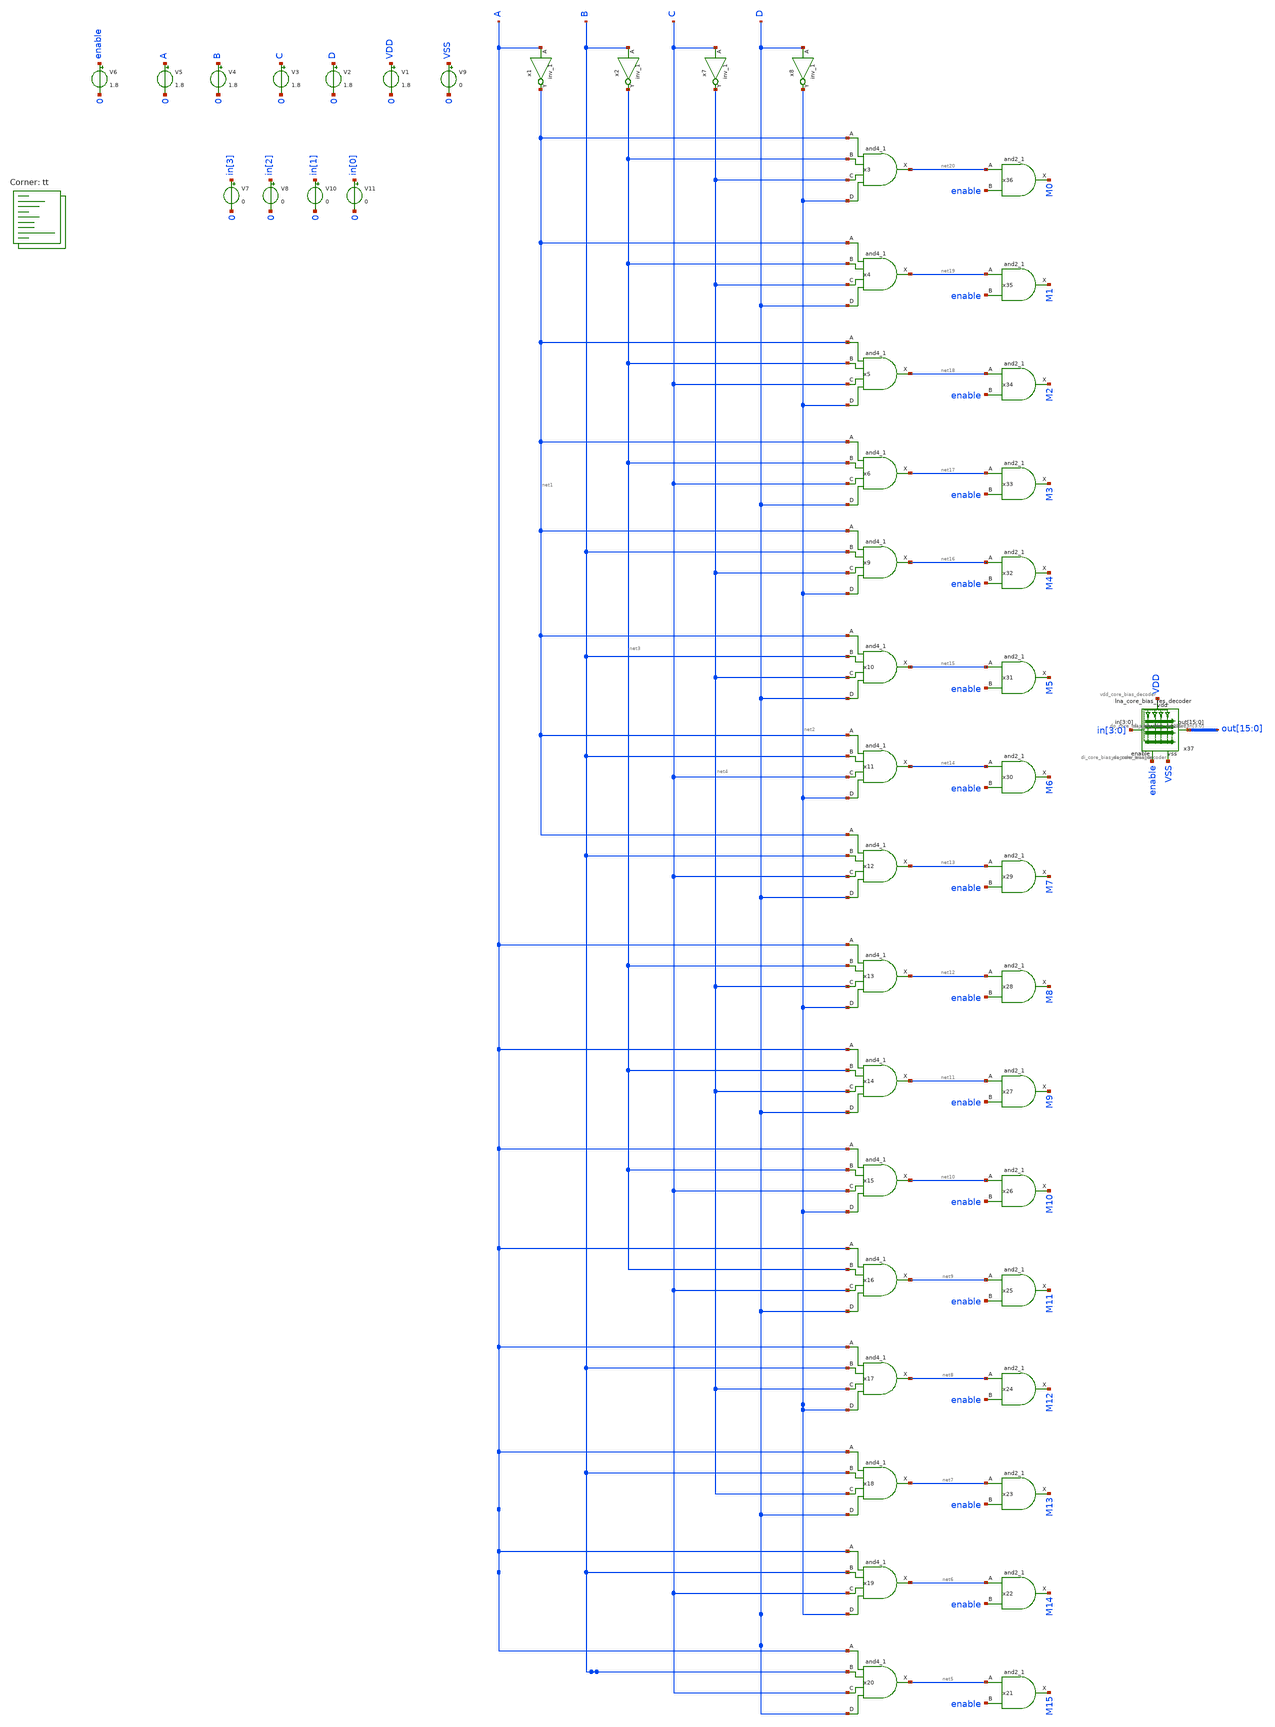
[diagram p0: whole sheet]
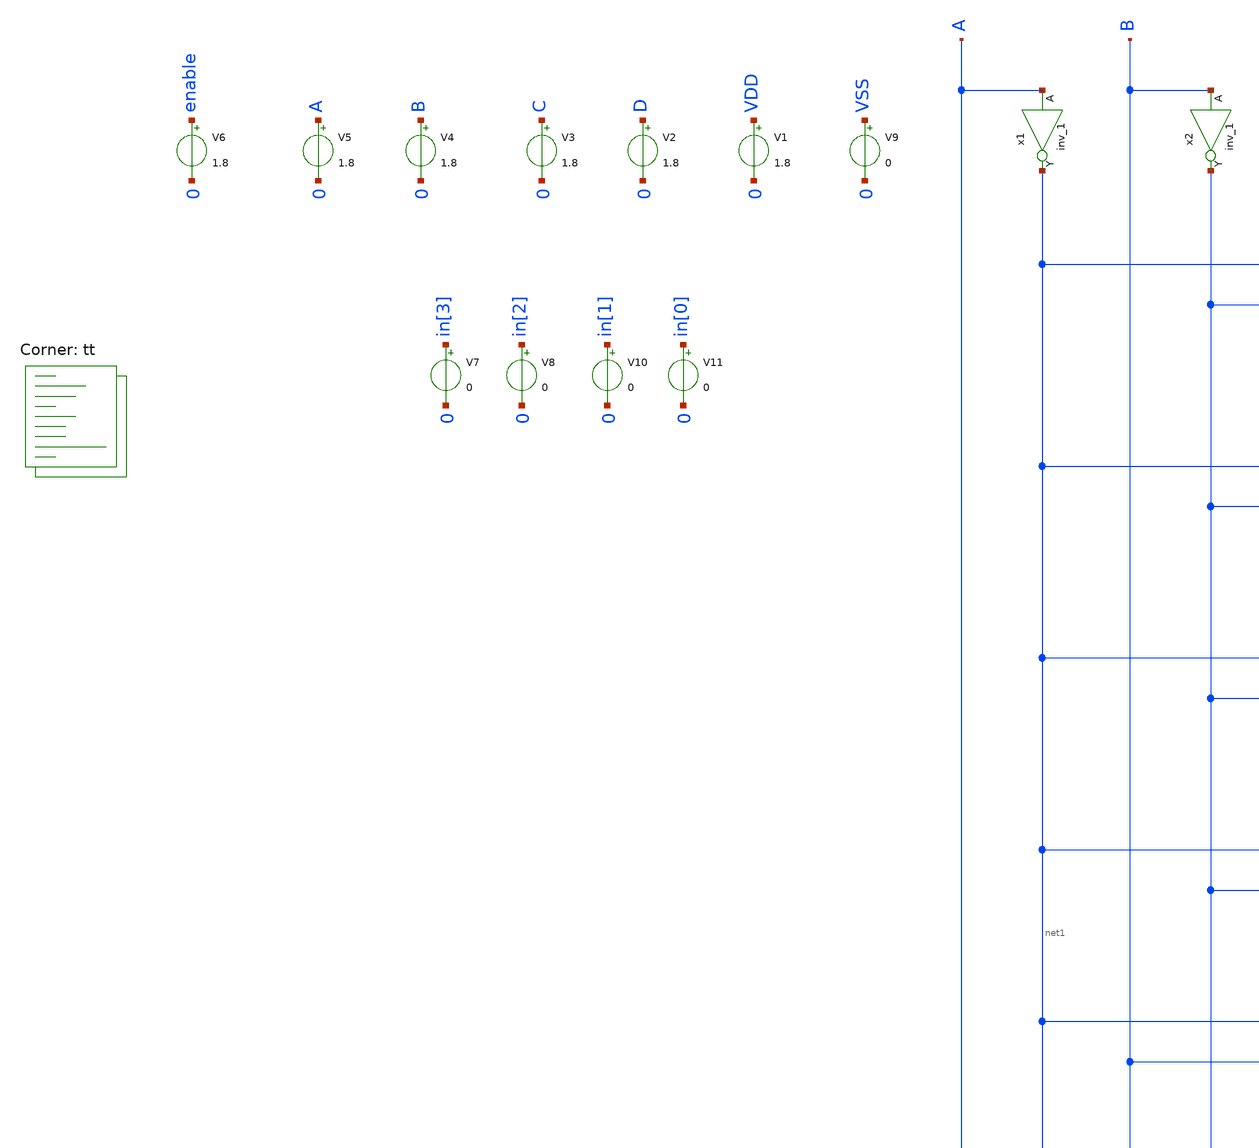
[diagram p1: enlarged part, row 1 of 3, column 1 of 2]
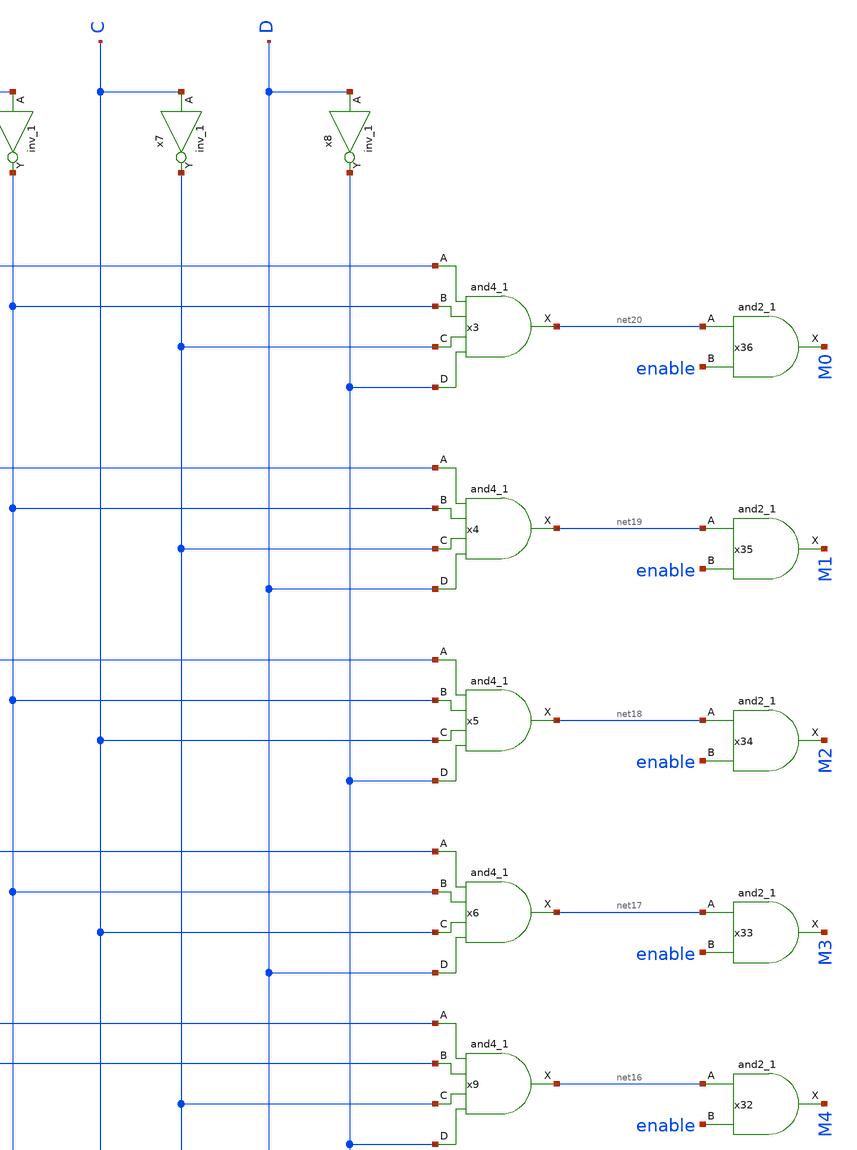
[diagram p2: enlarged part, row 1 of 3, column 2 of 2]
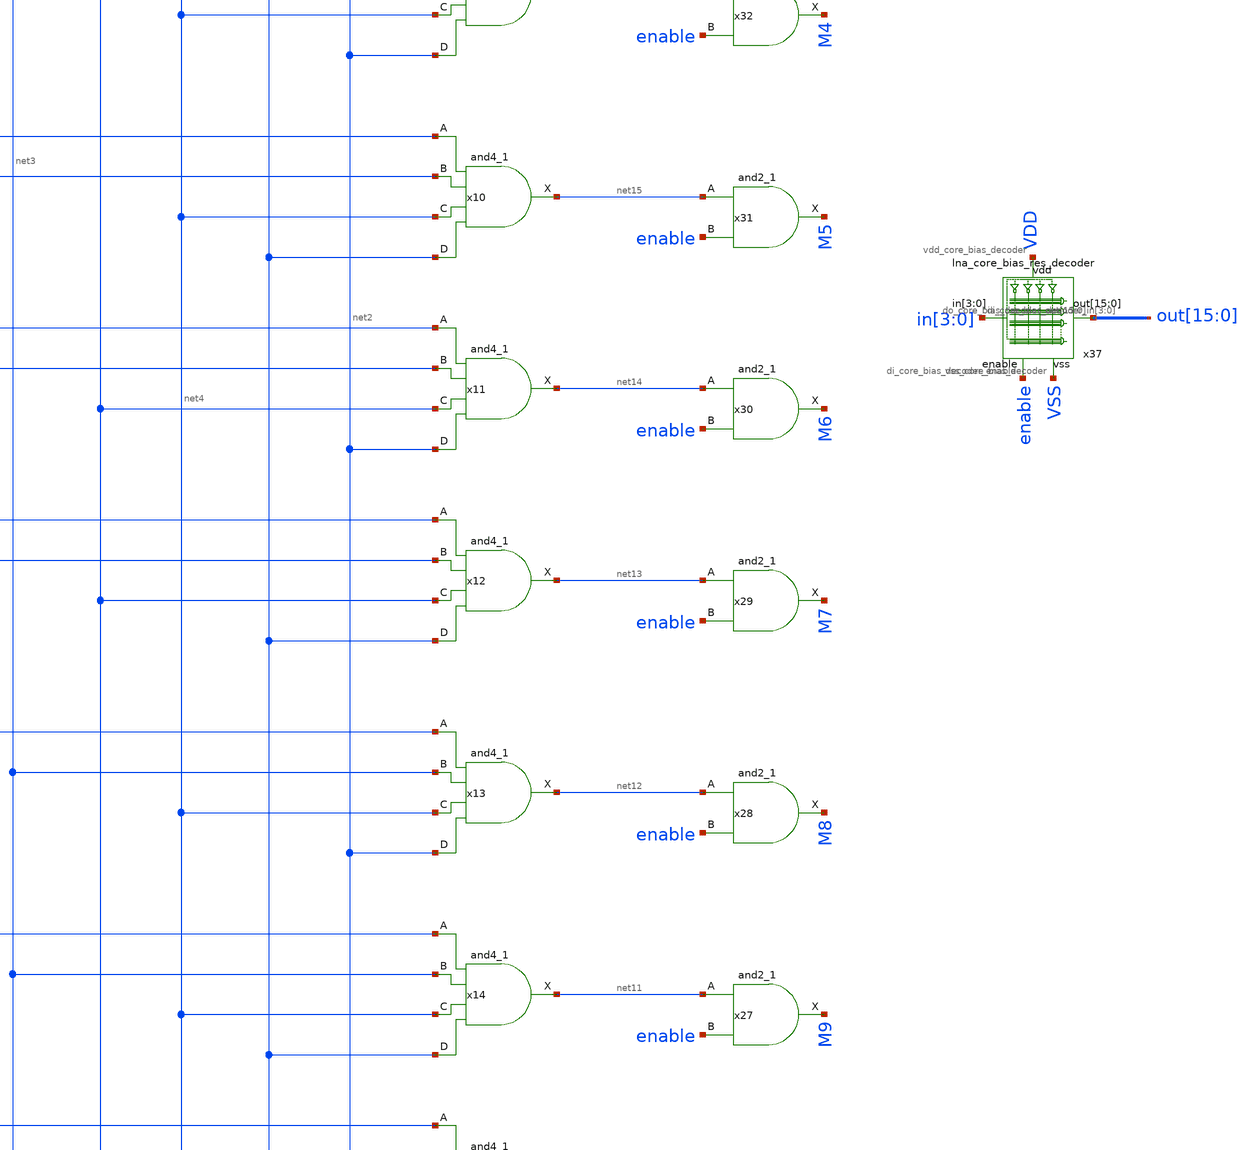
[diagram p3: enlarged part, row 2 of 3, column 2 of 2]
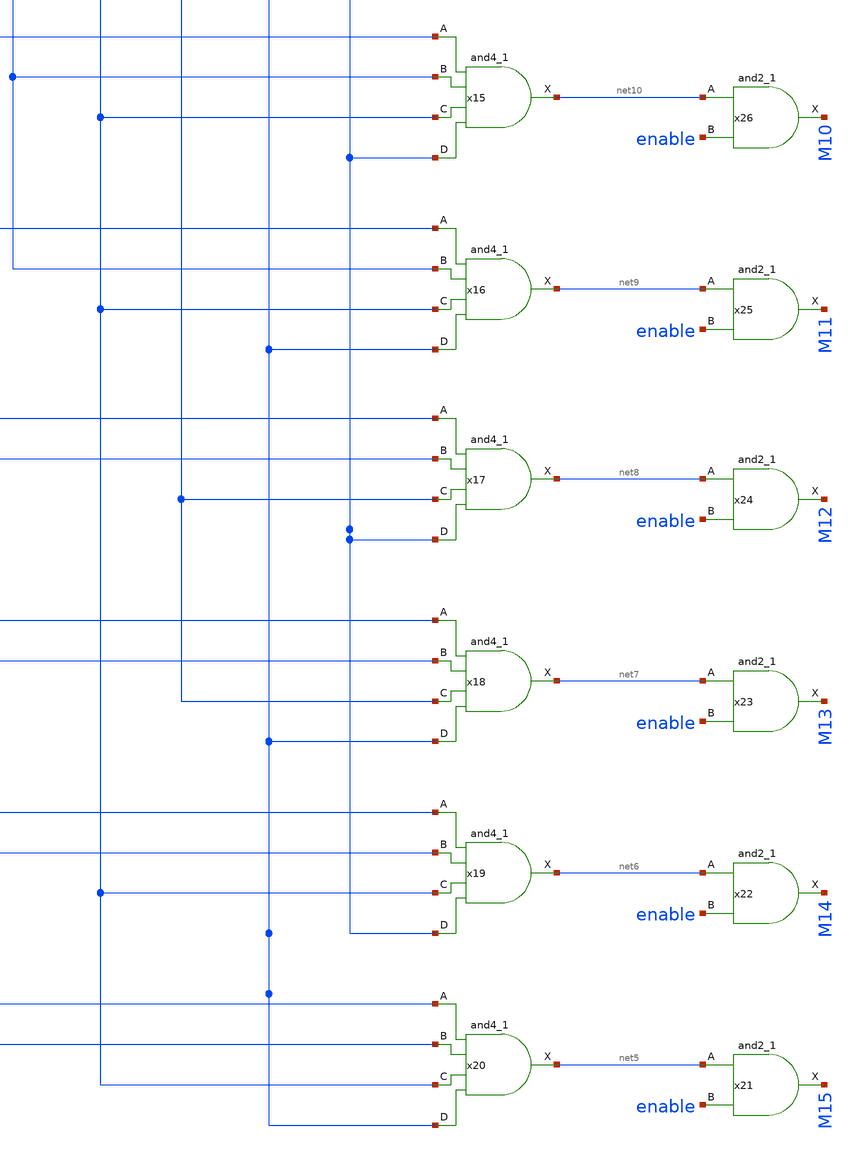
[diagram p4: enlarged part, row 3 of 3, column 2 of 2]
** sch_path: testbench_decoder.sch
**.subckt testbench_decoder
x1 A VSS VSS VDD VDD net1 sky130_fd_sc_hd__inv_1
x2 B VSS VSS VDD VDD net3 sky130_fd_sc_hd__inv_1
x7 C VSS VSS VDD VDD net4 sky130_fd_sc_hd__inv_1
x8 D VSS VSS VDD VDD net2 sky130_fd_sc_hd__inv_1
x3 net1 net3 net4 net2 VSS VSS VDD VDD net20 sky130_fd_sc_hd__and4_1
x4 net1 net3 net4 D VSS VSS VDD VDD net19 sky130_fd_sc_hd__and4_1
x5 net1 net3 C net2 VSS VSS VDD VDD net18 sky130_fd_sc_hd__and4_1
x6 net1 net3 C D VSS VSS VDD VDD net17 sky130_fd_sc_hd__and4_1
x9 net1 B net4 net2 VSS VSS VDD VDD net16 sky130_fd_sc_hd__and4_1
x10 net1 B net4 D VSS VSS VDD VDD net15 sky130_fd_sc_hd__and4_1
x11 net1 B C net2 VSS VSS VDD VDD net14 sky130_fd_sc_hd__and4_1
x12 net1 B C D VSS VSS VDD VDD net13 sky130_fd_sc_hd__and4_1
x13 A net3 net4 net2 VSS VSS VDD VDD net12 sky130_fd_sc_hd__and4_1
x14 A net3 net4 D VSS VSS VDD VDD net11 sky130_fd_sc_hd__and4_1
x15 A net3 C net2 VSS VSS VDD VDD net10 sky130_fd_sc_hd__and4_1
x16 A net3 C D VSS VSS VDD VDD net9 sky130_fd_sc_hd__and4_1
x17 A B net4 net2 VSS VSS VDD VDD net8 sky130_fd_sc_hd__and4_1
x18 A B net4 D VSS VSS VDD VDD net7 sky130_fd_sc_hd__and4_1
x19 A B C net2 VSS VSS VDD VDD net6 sky130_fd_sc_hd__and4_1
x20 A B C D VSS VSS VDD VDD net5 sky130_fd_sc_hd__and4_1
V9 VSS 0 0
V1 VDD 0 1.8
V2 D 0 1.8
V3 C 0 1.8
V4 B 0 1.8
V5 A 0 1.8
x21 net5 enable VSS VSS VDD VDD M15 sky130_fd_sc_hd__and2_1
V6 enable 0 1.8
x22 net6 enable VSS VSS VDD VDD M14 sky130_fd_sc_hd__and2_1
x23 net7 enable VSS VSS VDD VDD M13 sky130_fd_sc_hd__and2_1
x24 net8 enable VSS VSS VDD VDD M12 sky130_fd_sc_hd__and2_1
x25 net9 enable VSS VSS VDD VDD M11 sky130_fd_sc_hd__and2_1
x26 net10 enable VSS VSS VDD VDD M10 sky130_fd_sc_hd__and2_1
x27 net11 enable VSS VSS VDD VDD M9 sky130_fd_sc_hd__and2_1
x28 net12 enable VSS VSS VDD VDD M8 sky130_fd_sc_hd__and2_1
x29 net13 enable VSS VSS VDD VDD M7 sky130_fd_sc_hd__and2_1
x30 net14 enable VSS VSS VDD VDD M6 sky130_fd_sc_hd__and2_1
x31 net15 enable VSS VSS VDD VDD M5 sky130_fd_sc_hd__and2_1
x32 net16 enable VSS VSS VDD VDD M4 sky130_fd_sc_hd__and2_1
x33 net17 enable VSS VSS VDD VDD M3 sky130_fd_sc_hd__and2_1
x34 net18 enable VSS VSS VDD VDD M2 sky130_fd_sc_hd__and2_1
x35 net19 enable VSS VSS VDD VDD M1 sky130_fd_sc_hd__and2_1
x36 net20 enable VSS VSS VDD VDD M0 sky130_fd_sc_hd__and2_1
V7 in[3] 0 0
V8 in[2] 0 0
V10 in[1] 0 0
V11 in[0] 0 0
x37 in[3] in[2] in[1] in[0] out[15] out[14] out[13] out[12] out[11] out[10] out[9] out[8] out[7]
+ out[6] out[5] out[4] out[3] out[2] out[1] out[0] VDD VSS enable lna_core_bias_res_decoder
**** begin user architecture code
.lib $::SKYWATER_MODELS/sky130.lib.spice tt


.tran 10u 1m
.save all



.include $::SKYWATER_STDCELLS/sky130_fd_sc_hd.spice

**** end user architecture code
**.ends

* expanding   symbol:  LNA/lna_core_bias_res_decoder.sym # of pins=5
** sym_path: lna_core_bias_res_decoder.sym
** sch_path: lna_core_bias_res_decoder.sch
.subckt lna_core_bias_res_decoder di_core_bias_decoder_in[3] di_core_bias_decoder_in[2]
+ di_core_bias_decoder_in[1] di_core_bias_decoder_in[0] do_core_bias_decoder_out[15] do_core_bias_decoder_out[14]
+ do_core_bias_decoder_out[13] do_core_bias_decoder_out[12] do_core_bias_decoder_out[11] do_core_bias_decoder_out[10]
+ do_core_bias_decoder_out[9] do_core_bias_decoder_out[8] do_core_bias_decoder_out[7] do_core_bias_decoder_out[6]
+ do_core_bias_decoder_out[5] do_core_bias_decoder_out[4] do_core_bias_decoder_out[3] do_core_bias_decoder_out[2]
+ do_core_bias_decoder_out[1] do_core_bias_decoder_out[0] vdd_core_bias_decoder vss_core_bias_decoder di_core_bias_decoder_enable
*.opin
*+ do_core_bias_decoder_out[15],do_core_bias_decoder_out[14],do_core_bias_decoder_out[13],do_core_bias_decoder_out[12],do_core_bias_decoder_out[11],do_core_bias_decoder_out[10],do_core_bias_decoder_out[9],do_core_bias_decoder_out[8],do_core_bias_decoder_out[7],do_core_bias_decoder_out[6],do_core_bias_decoder_out[5],do_core_bias_decoder_out[4],do_core_bias_decoder_out[3],do_core_bias_decoder_out[2],do_core_bias_decoder_out[1],do_core_bias_decoder_out[0]
*.ipin
*+ di_core_bias_decoder_in[3],di_core_bias_decoder_in[2],di_core_bias_decoder_in[1],di_core_bias_decoder_in[0]
*.ipin di_core_bias_decoder_enable
*.ipin vdd_core_bias_decoder
*.ipin vss_core_bias_decoder
x1 di_core_bias_decoder_in[3] vss_core_bias_decoder vss_core_bias_decoder vdd_core_bias_decoder
+ vdd_core_bias_decoder net1 sky130_fd_sc_hd__inv_1
x2 di_core_bias_decoder_in[2] vss_core_bias_decoder vss_core_bias_decoder vdd_core_bias_decoder
+ vdd_core_bias_decoder net3 sky130_fd_sc_hd__inv_1
x7 di_core_bias_decoder_in[1] vss_core_bias_decoder vss_core_bias_decoder vdd_core_bias_decoder
+ vdd_core_bias_decoder net4 sky130_fd_sc_hd__inv_1
x8 di_core_bias_decoder_in[0] vss_core_bias_decoder vss_core_bias_decoder vdd_core_bias_decoder
+ vdd_core_bias_decoder net2 sky130_fd_sc_hd__inv_1
x3 net1 net3 net4 net2 vss_core_bias_decoder vss_core_bias_decoder vdd_core_bias_decoder
+ vdd_core_bias_decoder net20 sky130_fd_sc_hd__and4_1
x4 net1 net3 net4 di_core_bias_decoder_in[0] vss_core_bias_decoder vss_core_bias_decoder
+ vdd_core_bias_decoder vdd_core_bias_decoder net19 sky130_fd_sc_hd__and4_1
x5 net1 net3 di_core_bias_decoder_in[1] net2 vss_core_bias_decoder vss_core_bias_decoder
+ vdd_core_bias_decoder vdd_core_bias_decoder net18 sky130_fd_sc_hd__and4_1
x6 net1 net3 di_core_bias_decoder_in[1] di_core_bias_decoder_in[0] vss_core_bias_decoder
+ vss_core_bias_decoder vdd_core_bias_decoder vdd_core_bias_decoder net17 sky130_fd_sc_hd__and4_1
x9 net1 di_core_bias_decoder_in[2] net4 net2 vss_core_bias_decoder vss_core_bias_decoder
+ vdd_core_bias_decoder vdd_core_bias_decoder net16 sky130_fd_sc_hd__and4_1
x10 net1 di_core_bias_decoder_in[2] net4 di_core_bias_decoder_in[0] vss_core_bias_decoder
+ vss_core_bias_decoder vdd_core_bias_decoder vdd_core_bias_decoder net15 sky130_fd_sc_hd__and4_1
x11 net1 di_core_bias_decoder_in[2] di_core_bias_decoder_in[1] net2 vss_core_bias_decoder
+ vss_core_bias_decoder vdd_core_bias_decoder vdd_core_bias_decoder net14 sky130_fd_sc_hd__and4_1
x12 net1 di_core_bias_decoder_in[2] di_core_bias_decoder_in[1] di_core_bias_decoder_in[0]
+ vss_core_bias_decoder vss_core_bias_decoder vdd_core_bias_decoder vdd_core_bias_decoder net13 sky130_fd_sc_hd__and4_1
x13 di_core_bias_decoder_in[3] net3 net4 net2 vss_core_bias_decoder vss_core_bias_decoder
+ vdd_core_bias_decoder vdd_core_bias_decoder net12 sky130_fd_sc_hd__and4_1
x14 di_core_bias_decoder_in[3] net3 net4 di_core_bias_decoder_in[0] vss_core_bias_decoder
+ vss_core_bias_decoder vdd_core_bias_decoder vdd_core_bias_decoder net11 sky130_fd_sc_hd__and4_1
x15 di_core_bias_decoder_in[3] net3 di_core_bias_decoder_in[1] net2 vss_core_bias_decoder
+ vss_core_bias_decoder vdd_core_bias_decoder vdd_core_bias_decoder net10 sky130_fd_sc_hd__and4_1
x16 di_core_bias_decoder_in[3] net3 di_core_bias_decoder_in[1] di_core_bias_decoder_in[0]
+ vss_core_bias_decoder vss_core_bias_decoder vdd_core_bias_decoder vdd_core_bias_decoder net9 sky130_fd_sc_hd__and4_1
x17 di_core_bias_decoder_in[3] di_core_bias_decoder_in[2] net4 net2 vss_core_bias_decoder
+ vss_core_bias_decoder vdd_core_bias_decoder vdd_core_bias_decoder net8 sky130_fd_sc_hd__and4_1
x18 di_core_bias_decoder_in[3] di_core_bias_decoder_in[2] net4 di_core_bias_decoder_in[0]
+ vss_core_bias_decoder vss_core_bias_decoder vdd_core_bias_decoder vdd_core_bias_decoder net7 sky130_fd_sc_hd__and4_1
x19 di_core_bias_decoder_in[3] di_core_bias_decoder_in[2] di_core_bias_decoder_in[1] net2
+ vss_core_bias_decoder vss_core_bias_decoder vdd_core_bias_decoder vdd_core_bias_decoder net6 sky130_fd_sc_hd__and4_1
x20 di_core_bias_decoder_in[3] di_core_bias_decoder_in[2] di_core_bias_decoder_in[1]
+ di_core_bias_decoder_in[0] vss_core_bias_decoder vss_core_bias_decoder vdd_core_bias_decoder vdd_core_bias_decoder net5
+ sky130_fd_sc_hd__and4_1
x21 net5 di_core_bias_decoder_enable vss_core_bias_decoder vss_core_bias_decoder
+ vdd_core_bias_decoder vdd_core_bias_decoder do_core_bias_decoder_out[15] sky130_fd_sc_hd__and2_1
x22 net6 di_core_bias_decoder_enable vss_core_bias_decoder vss_core_bias_decoder
+ vdd_core_bias_decoder vdd_core_bias_decoder do_core_bias_decoder_out[14] sky130_fd_sc_hd__and2_1
x23 net7 di_core_bias_decoder_enable vss_core_bias_decoder vss_core_bias_decoder
+ vdd_core_bias_decoder vdd_core_bias_decoder do_core_bias_decoder_out[13] sky130_fd_sc_hd__and2_1
x24 net8 di_core_bias_decoder_enable vss_core_bias_decoder vss_core_bias_decoder
+ vdd_core_bias_decoder vdd_core_bias_decoder do_core_bias_decoder_out[12] sky130_fd_sc_hd__and2_1
x25 net9 di_core_bias_decoder_enable vss_core_bias_decoder vss_core_bias_decoder
+ vdd_core_bias_decoder vdd_core_bias_decoder do_core_bias_decoder_out[11] sky130_fd_sc_hd__and2_1
x26 net10 di_core_bias_decoder_enable vss_core_bias_decoder vss_core_bias_decoder
+ vdd_core_bias_decoder vdd_core_bias_decoder do_core_bias_decoder_out[10] sky130_fd_sc_hd__and2_1
x27 net11 di_core_bias_decoder_enable vss_core_bias_decoder vss_core_bias_decoder
+ vdd_core_bias_decoder vdd_core_bias_decoder do_core_bias_decoder_out[9] sky130_fd_sc_hd__and2_1
x28 net12 di_core_bias_decoder_enable vss_core_bias_decoder vss_core_bias_decoder
+ vdd_core_bias_decoder vdd_core_bias_decoder do_core_bias_decoder_out[8] sky130_fd_sc_hd__and2_1
x29 net13 di_core_bias_decoder_enable vss_core_bias_decoder vss_core_bias_decoder
+ vdd_core_bias_decoder vdd_core_bias_decoder do_core_bias_decoder_out[7] sky130_fd_sc_hd__and2_1
x30 net14 di_core_bias_decoder_enable vss_core_bias_decoder vss_core_bias_decoder
+ vdd_core_bias_decoder vdd_core_bias_decoder do_core_bias_decoder_out[6] sky130_fd_sc_hd__and2_1
x31 net15 di_core_bias_decoder_enable vss_core_bias_decoder vss_core_bias_decoder
+ vdd_core_bias_decoder vdd_core_bias_decoder do_core_bias_decoder_out[5] sky130_fd_sc_hd__and2_1
x32 net16 di_core_bias_decoder_enable vss_core_bias_decoder vss_core_bias_decoder
+ vdd_core_bias_decoder vdd_core_bias_decoder do_core_bias_decoder_out[4] sky130_fd_sc_hd__and2_1
x33 net17 di_core_bias_decoder_enable vss_core_bias_decoder vss_core_bias_decoder
+ vdd_core_bias_decoder vdd_core_bias_decoder do_core_bias_decoder_out[3] sky130_fd_sc_hd__and2_1
x34 net18 di_core_bias_decoder_enable vss_core_bias_decoder vss_core_bias_decoder
+ vdd_core_bias_decoder vdd_core_bias_decoder do_core_bias_decoder_out[2] sky130_fd_sc_hd__and2_1
x35 net19 di_core_bias_decoder_enable vss_core_bias_decoder vss_core_bias_decoder
+ vdd_core_bias_decoder vdd_core_bias_decoder do_core_bias_decoder_out[1] sky130_fd_sc_hd__and2_1
x36 net20 di_core_bias_decoder_enable vss_core_bias_decoder vss_core_bias_decoder
+ vdd_core_bias_decoder vdd_core_bias_decoder do_core_bias_decoder_out[0] sky130_fd_sc_hd__and2_1
.ends

.end
